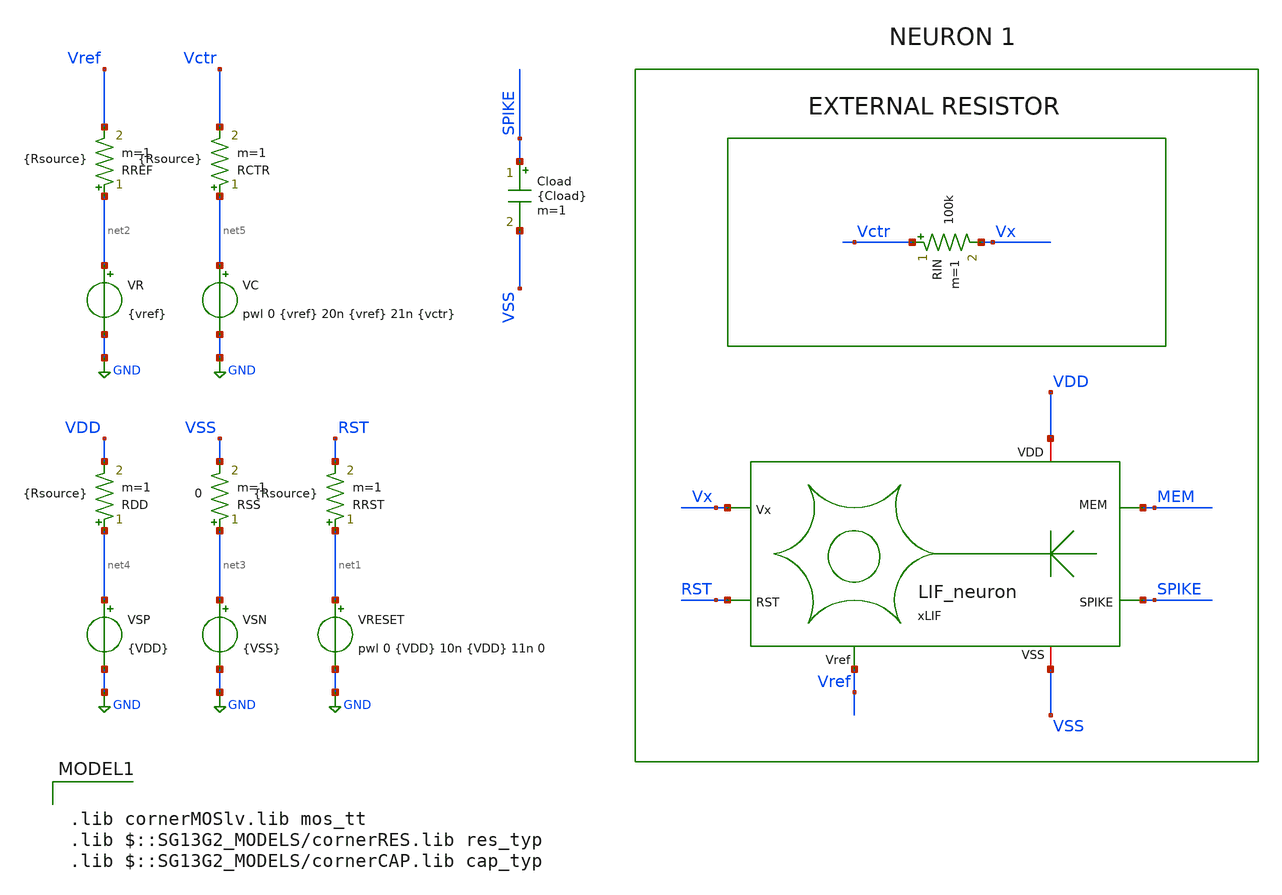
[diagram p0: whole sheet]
** sch_path: work/LIF_Neuron/xschem/LIF_neuron_tb.sch
**.subckt LIF_neuron_tb
VRESET net1 GND pwl 0 {VDD} 10n {VDD} 11n 0
VSP net4 GND {VDD}
VSN net3 GND {VSS}
VR net2 GND {vref}
VC net5 GND pwl 0 {vref} 20n {vref} 21n {vctr}
xLIF VDD Vx MEM RST SPIKE VSS Vref LIF_neuron
RDD net4 VDD {Rsource} m=1
RSS net3 VSS 0 m=1
RRST net1 RST {Rsource} m=1
RREF net2 Vref {Rsource} m=1
RCTR net5 Vctr {Rsource} m=1
Cload SPIKE VSS {Cload} m=1
RIN Vctr Vx 100k m=1
**** begin user architecture code



.param VDD = 1.2
.param VSS = 0
.param vctr = 1
.param vref = 0
.param Cload = 0.1p
.param Rsource = 10

.param sw_stat_global = 0
.param sw_stat_mismatch = 0

.save all

.control

* >> Variables <<
let Vhigh = 0.8
let Vmid = Vhigh * 0.5

let tstop = 50n
let tstep = tstop/1k

* Run transient analysis
tran $&tstep $&tstop

let IDD = -1*i(VSP)
meas tran I_avg AVG IDD from=tstep to=tstop
let P_avg = abs(I_avg*Vhigh)

meas TRAN T_spk TRIG v(SPIKE) VAL=Vmid rise=2 TARG v(SPIKE) VAL=Vmid rise=3
let F_spk = 1 / T_spk

let E_spk = P_avg/F_spk

*Print results
print F_spk I_avg P_avg E_spk

* Plots
plot v(Vctr) v(Vref) v(RST)
plot v(MEM) v(Vx)
plot v(xLIF.COMP)
plot v(SPIKE)

.endc



.lib cornerMOSlv.lib mos_tt
.lib $::SG13G2_MODELS/cornerRES.lib res_typ
.lib $::SG13G2_MODELS/cornerCAP.lib cap_typ

**** end user architecture code
**.ends
.GLOBAL GND
.end
